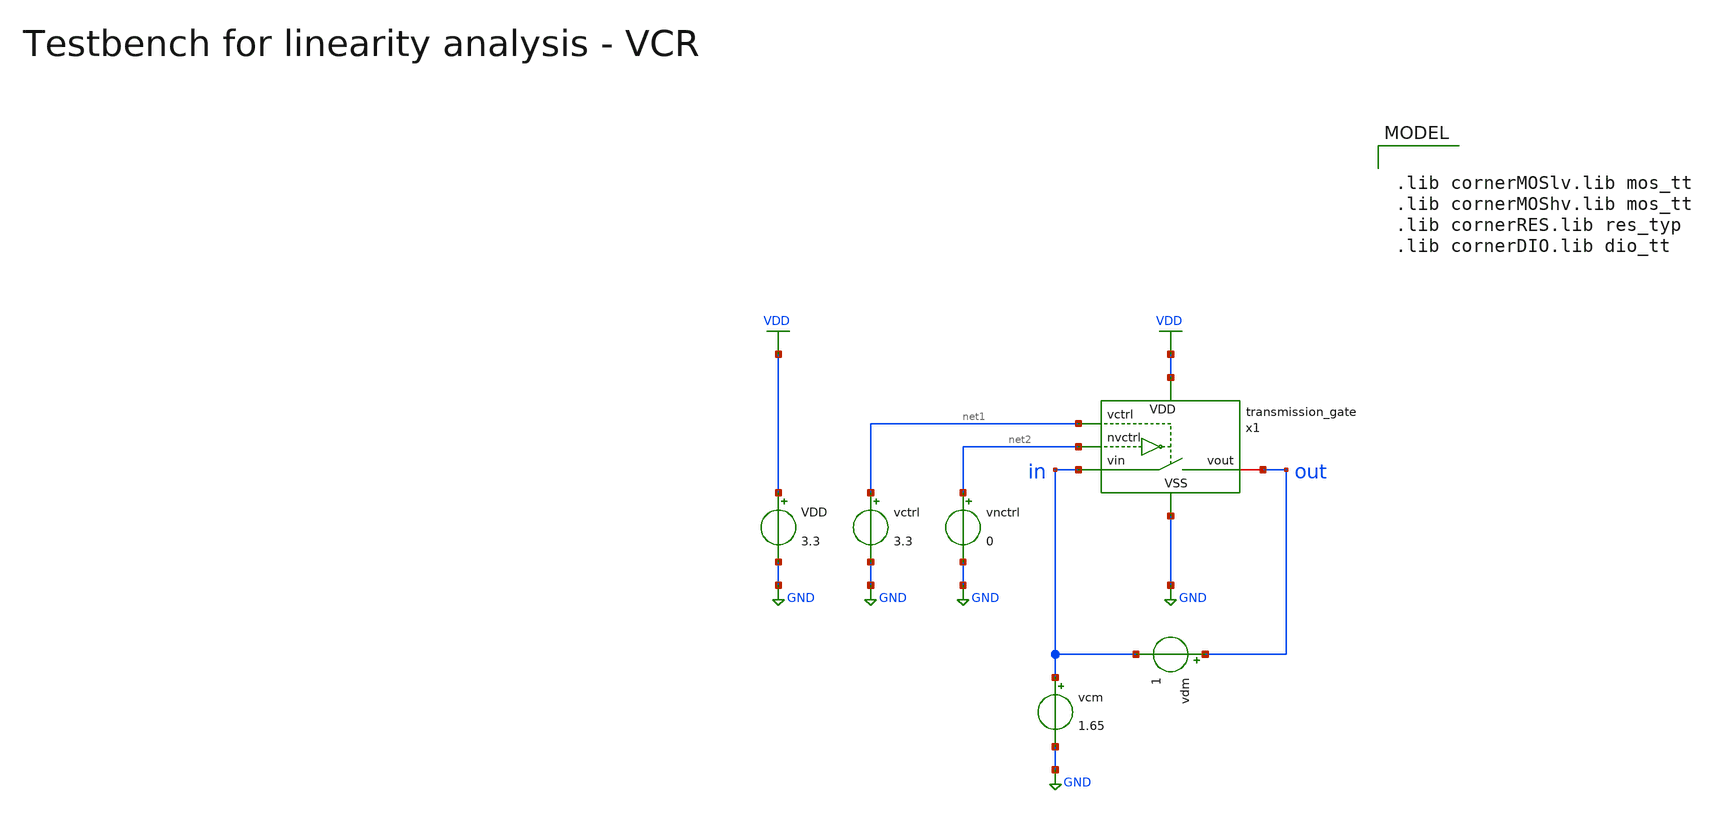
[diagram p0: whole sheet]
** sch_path: macros/heichips26_vcr/macros/switched_capacitor/testbenches/xschem/tb_transmission_gate_linearity_dc.sch
**.subckt tb_transmission_gate_linearity_dc
VDD VDD GND 3.3
vcm in GND 1.65
vctrl net1 GND 3.3
x1 net1 in out net2 VDD GND transmission_gate
vnctrl net2 GND 0
vdm out in 1
**** begin user architecture code

.lib cornerMOSlv.lib mos_tt
.lib cornerMOShv.lib mos_tt
.lib cornerRES.lib res_typ
.lib cornerDIO.lib dio_tt



.param temp=27

* Derived timing parameters

.options savecurrents klu method=gear reltol=1e-3 abstol=1e-15 gmin=1e-15
.probe alli
.control

unset appendwrite
set wr_vecnames
set wr_singlescale

echo
echo # ------------------------------------------------------------------------------
echo # VCM sweep:
echo # ------------------------------------------------------------------------------
echo

dc vcm -1 3.3 0.05 vdm 0.1 2.1 0.5
let vcm = (out+in)/2
let R = (in-out)/i(vdm)
plot R vs vcm
wrdata ../plot_simulations/data/@schname\_vcm.txt in out i(vdm)

echo
echo # ------------------------------------------------------------------------------
echo # VDM sweep:
echo # ------------------------------------------------------------------------------
echo

dc vdm -3.3 3.3 0.052 vcm 0.65 2.65 0.5
let vdm = out-in
let R = (in-out)/i(vdm)
plot R vs vdm
wrdata ../plot_simulations/data/@schname\_vdm.txt in out i(vdm)

.endc


**** end user architecture code
**.ends

* expanding   symbol:  transmission_gate.sym # of pins=6
** sym_path: macros/heichips26_vcr/macros/switched_capacitor/schematic/xschem/transmission_gate.sym
** sch_path: macros/heichips26_vcr/macros/switched_capacitor/schematic/xschem/transmission_gate.sch
.subckt transmission_gate vctrl vin vout nvctrl VDD VSS
*.iopin vin
*.iopin vout
*.ipin vctrl
*.ipin nvctrl
*.iopin VDD
*.iopin VSS
XM3 vout vctrl vin VSS sg13_hv_nmos w={tg_ngate_w*tg_ng} l={tg_ch_len} ng={tg_ng} m=1 mm_ok=1
XM4 vout nvctrl vin VDD sg13_hv_pmos w={tg_pgate_w*tg_ng} l={tg_ch_len} ng={tg_ng} m=1 mm_ok=1
**** begin user architecture code


.param tg_ch_len=0.45u
.param tg_ngate_w=2u
.param tg_pgate_w=5u
.param tg_ng=20


**** end user architecture code
.ends

.GLOBAL GND
.GLOBAL VDD
.end
